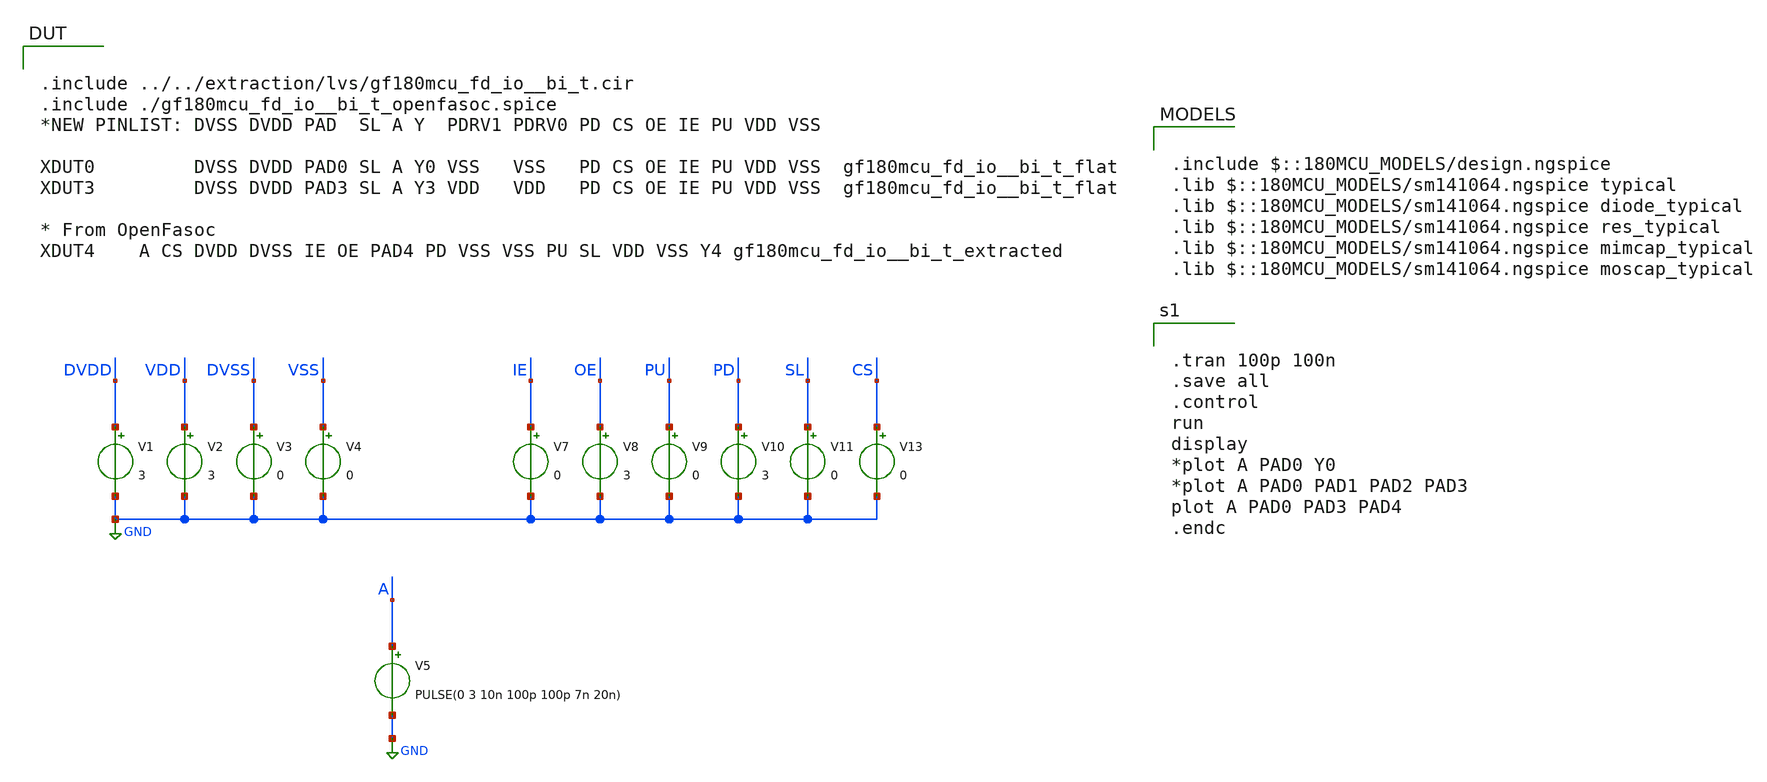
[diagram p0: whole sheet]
** sch_path: test/bi_t_switch/bi_t_switch.sch
**.subckt bi_t_switch
V1 DVDD GND 3
V2 VDD GND 3
V3 DVSS GND 0
V4 VSS GND 0
V5 A GND PULSE(0 3 10n 100p 100p 7n 20n)
V7 IE GND 0
V8 OE GND 3
V9 PU GND 0
V10 PD GND 3
V11 SL GND 0
V13 CS GND 0
**** begin user architecture code


.tran 100p 100n
.save all
.control
run
display
*plot A PAD0 Y0
*plot A PAD0 PAD1 PAD2 PAD3
plot A PAD0 PAD3 PAD4
.endc



.include $::180MCU_MODELS/design.ngspice
.lib $::180MCU_MODELS/sm141064.ngspice typical
.lib $::180MCU_MODELS/sm141064.ngspice diode_typical
.lib $::180MCU_MODELS/sm141064.ngspice res_typical
.lib $::180MCU_MODELS/sm141064.ngspice mimcap_typical
.lib $::180MCU_MODELS/sm141064.ngspice moscap_typical


.include ../../extraction/lvs/gf180mcu_fd_io__bi_t.cir
.include ./gf180mcu_fd_io__bi_t_openfasoc.spice
*NEW PINLIST: DVSS DVDD PAD  SL A Y  PDRV1 PDRV0 PD CS OE IE PU VDD VSS

XDUT0         DVSS DVDD PAD0 SL A Y0 VSS   VSS   PD CS OE IE PU VDD VSS  gf180mcu_fd_io__bi_t_flat
XDUT3         DVSS DVDD PAD3 SL A Y3 VDD   VDD   PD CS OE IE PU VDD VSS  gf180mcu_fd_io__bi_t_flat

* From OpenFasoc
XDUT4    A CS DVDD DVSS IE OE PAD4 PD VSS VSS PU SL VDD VSS Y4 gf180mcu_fd_io__bi_t_extracted

**** end user architecture code
**.ends
.GLOBAL GND
.end
